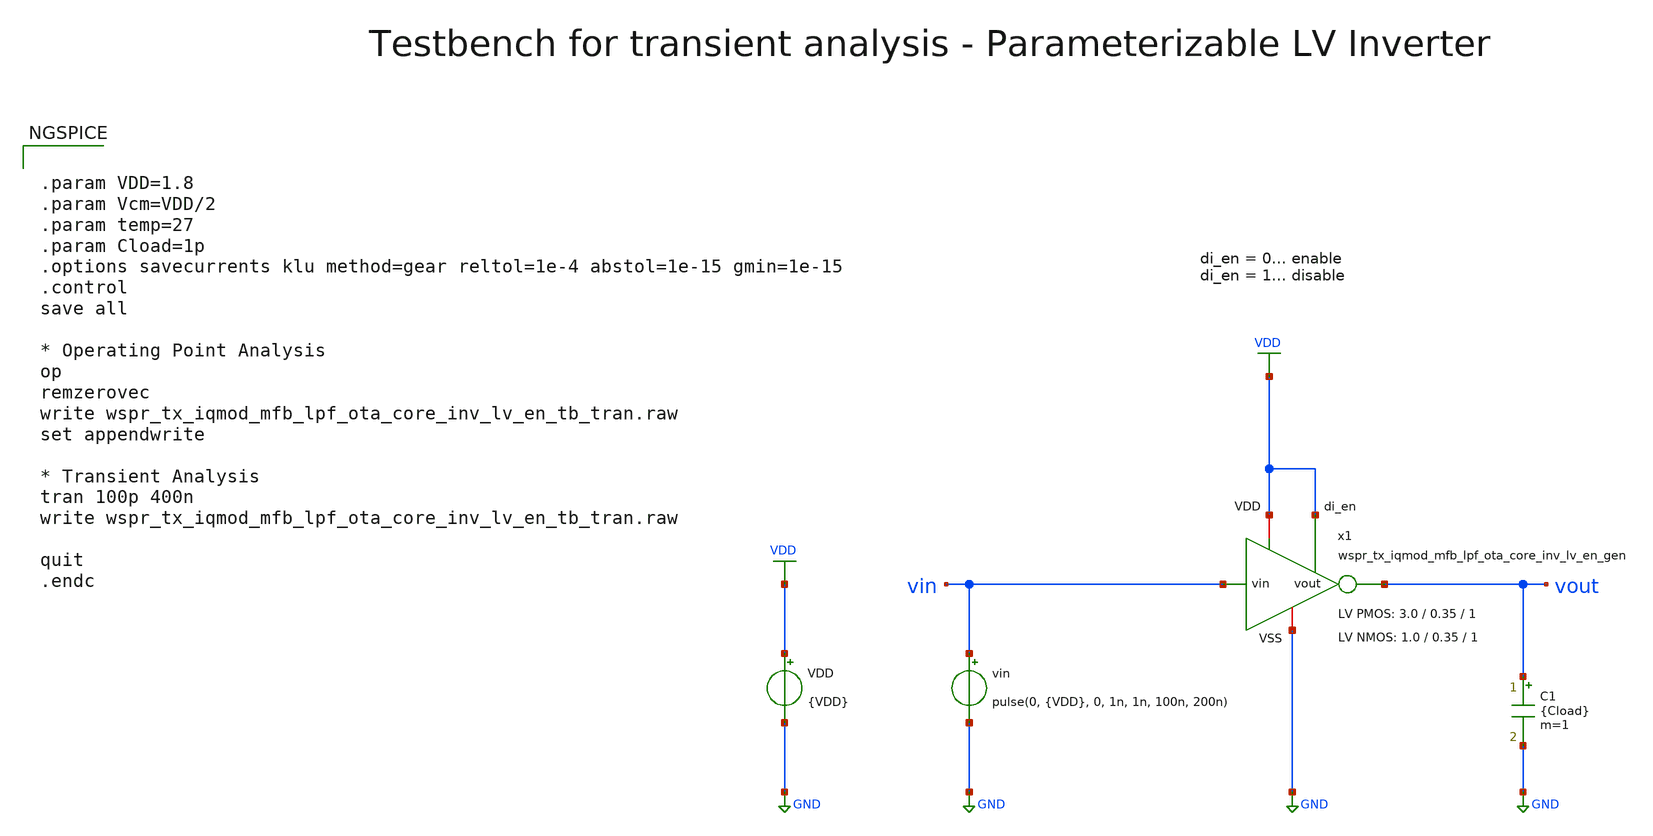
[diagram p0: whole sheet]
** sch_path: sky130/macros/iqmod/testbenches/wspr_tx_iqmod_mfb_lpf_ota_core_inv_lv_en_tb_tran.sch
**.subckt wspr_tx_iqmod_mfb_lpf_ota_core_inv_lv_en_tb_tran
VDD VDD GND {VDD}
vin vin GND pulse(0, {VDD}, 0, 1n, 1n, 100n, 200n)
C1 vout GND {Cload} m=1
x1 VDD vin vout GND VDD wspr_tx_iqmod_mfb_lpf_ota_core_inv_lv_en_gen W_P=3.0 L_P=0.35 NF_P=1 W_N=1.0
+ L_N=0.35 NF_N=1
**** begin user architecture code


.param VDD=1.8
.param Vcm=VDD/2
.param temp=27
.param Cload=1p
.options savecurrents klu method=gear reltol=1e-4 abstol=1e-15 gmin=1e-15
.control
save all

* Operating Point Analysis
op
remzerovec
write wspr_tx_iqmod_mfb_lpf_ota_core_inv_lv_en_tb_tran.raw
set appendwrite

* Transient Analysis
tran 100p 400n
write wspr_tx_iqmod_mfb_lpf_ota_core_inv_lv_en_tb_tran.raw

quit
.endc


.lib $::SKYWATER_MODELS/sky130.lib.spice tt
**** end user architecture code
**.ends

* expanding   symbol:  wspr_tx_iqmod_mfb_lpf_ota_core_inv_lv_en_gen.sym # of pins=7
** sym_path: sky130/xschem/generic/wspr_tx_iqmod_mfb_lpf_ota_core_inv_lv_en_gen.sym
** sch_path: sky130/xschem/generic/wspr_tx_iqmod_mfb_lpf_ota_core_inv_lv_en_gen.sch
.subckt wspr_tx_iqmod_mfb_lpf_ota_core_inv_lv_en_gen VDD vin vout VSS di_en  W_P=3.0 L_P=0.35 NF_P=1
+ W_N=1.0 L_N=0.35 NF_N=1
*.ipin vin
*.iopin VDD
*.iopin VSS
*.opin vout
*.ipin di_en
XM1 vout vin net1 VDD sky130_fd_pr__pfet_01v8_lvt L=L_P W=W_P nf=NF_P ad='int((NF_P + 1)/2) * W_P / NF_P * 0.29'
+ as='int((NF_P + 2)/2) * W_P / NF_P * 0.29' pd='2*int((NF_P + 1)/2) * (W_P / NF_P + 0.29)' ps='2*int((NF_P + 2)/2) * (W_P / NF_P + 0.29)'
+ nrd='0.29 / W_P ' nrs='0.29 / W_P ' sa=0 sb=0 sd=0 mult=1 m=1
XM3 net1 di_en VDD VDD sky130_fd_pr__pfet_01v8_lvt L=L_P W=W_P nf=2 ad='int((2 + 1)/2) * W_P / 2 * 0.29'
+ as='int((2 + 2)/2) * W_P / 2 * 0.29' pd='2*int((2 + 1)/2) * (W_P / 2 + 0.29)' ps='2*int((2 + 2)/2) * (W_P / 2 + 0.29)'
+ nrd='0.29 / W_P ' nrs='0.29 / W_P ' sa=0 sb=0 sd=0 mult=1 m=1
XM2 vout vin net2 VSS sky130_fd_pr__nfet_01v8_lvt L=L_N W=W_N nf=NF_N ad='int((NF_N + 1)/2) * W_N / NF_N * 0.29'
+ as='int((NF_N + 2)/2) * W_N / NF_N * 0.29' pd='2*int((NF_N + 1)/2) * (W_N / NF_N + 0.29)' ps='2*int((NF_N + 2)/2) * (W_N / NF_N + 0.29)'
+ nrd='0.29 / W_N ' nrs='0.29 / W_N ' sa=0 sb=0 sd=0 mult=1 m=1
XM4 net2 VDD VSS VSS sky130_fd_pr__nfet_01v8_lvt L=L_N W=W_N nf=2 ad='int((2 + 1)/2) * W_N / 2 * 0.29'
+ as='int((2 + 2)/2) * W_N / 2 * 0.29' pd='2*int((2 + 1)/2) * (W_N / 2 + 0.29)' ps='2*int((2 + 2)/2) * (W_N / 2 + 0.29)'
+ nrd='0.29 / W_N ' nrs='0.29 / W_N ' sa=0 sb=0 sd=0 mult=1 m=1
.ends

.GLOBAL GND
.GLOBAL VDD
.end
